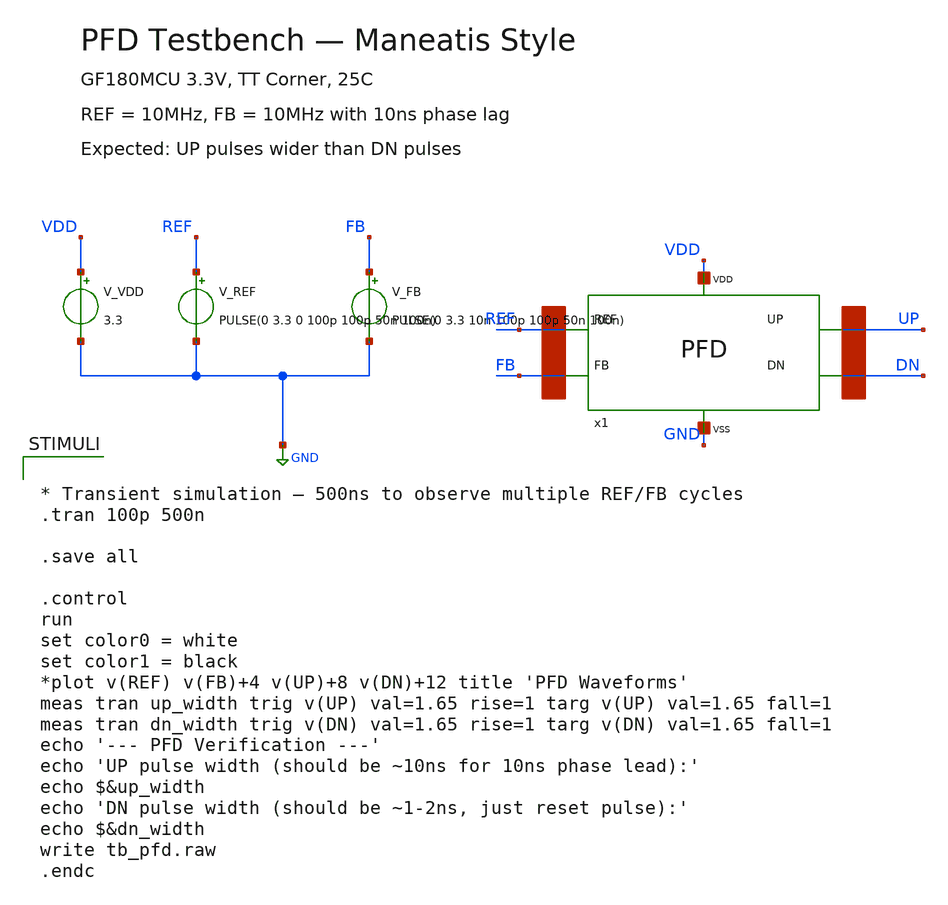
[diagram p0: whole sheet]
** sch_path: designs/libs/tb_analog/tb_pfd/tb_pfd.sch
**.subckt tb_pfd
V_REF REF GND PULSE(0 3.3 0 100p 100p 50n 100n)
V_FB FB GND PULSE(0 3.3 10n 100p 100p 50n 100n)
V_VDD VDD GND 3.3
x1 REF FB UP DN VDD GND pfd
**** begin user architecture code


* Transient simulation — 500ns to observe multiple REF/FB cycles
.tran 100p 500n

.save all

.control
run
set color0 = white
set color1 = black
*plot v(REF) v(FB)+4 v(UP)+8 v(DN)+12 title 'PFD Waveforms'
meas tran up_width trig v(UP) val=1.65 rise=1 targ v(UP) val=1.65 fall=1
meas tran dn_width trig v(DN) val=1.65 rise=1 targ v(DN) val=1.65 fall=1
echo '--- PFD Verification ---'
echo 'UP pulse width (should be ~10ns for 10ns phase lead):'
echo $&up_width
echo 'DN pulse width (should be ~1-2ns, just reset pulse):'
echo $&dn_width
write tb_pfd.raw
.endc



.include /foss/pdks/ciel/gf180mcu/versions/7b70722e33c03fcb5dabcf4d479fb0822d9251c9/gf180mcuD/libs.ref/gf180mcu_fd_sc_mcu7t5v0/spice/gf180mcu_fd_sc_mcu7t5v0.spice
.include $::180MCU_MODELS/design.ngspice
.lib $::180MCU_MODELS/sm141064.ngspice typical

**** end user architecture code
**.ends
.GLOBAL GND
.end
